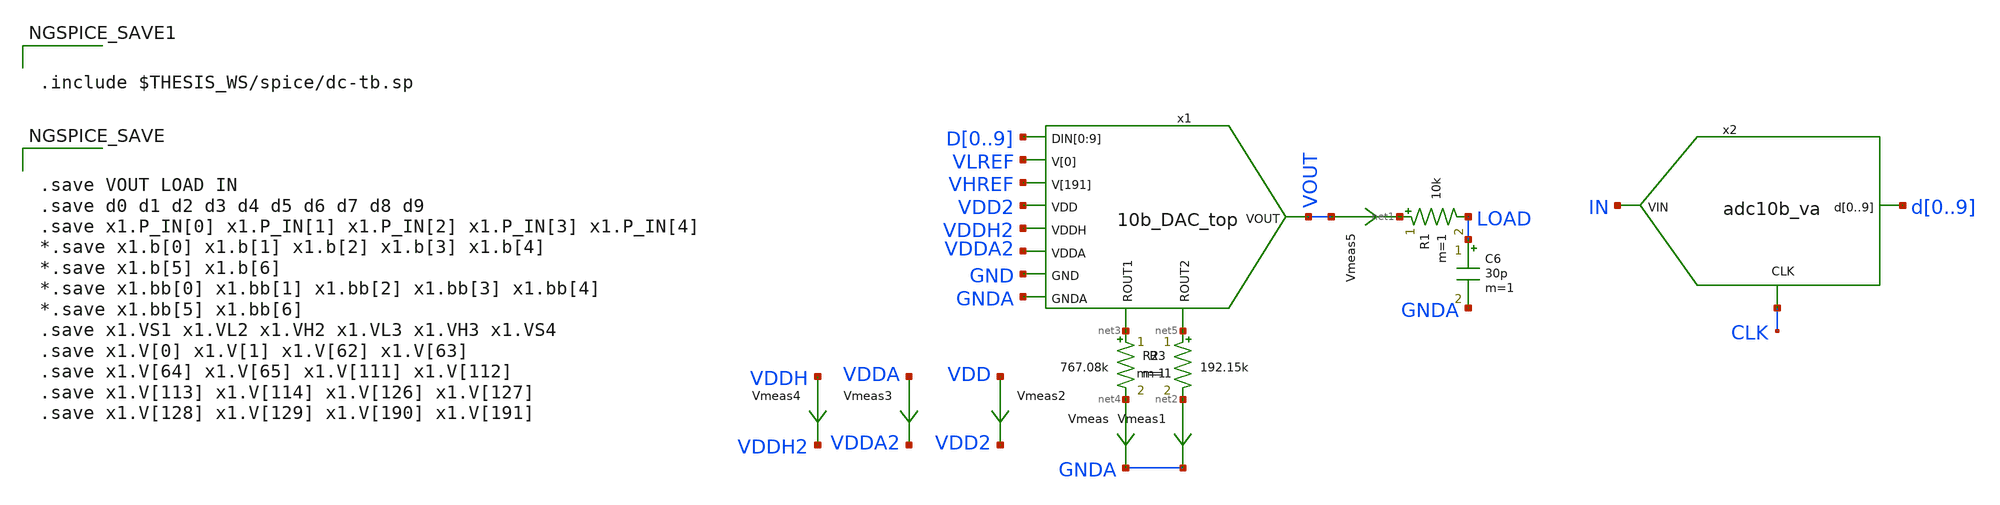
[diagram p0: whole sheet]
** sch_path: xschem/10b_DAC_dc-tb.sch
.lib $::SKYWATER_MODELS/sky130.lib.spice tt
.include $::SKYWATER_STDCELLS/sky130_fd_sc_hd.spice

**.subckt 10b_DAC_dc-tb
C6 LOAD GNDA 30p m=1
R1 net1 LOAD 10k m=1
Vmeas1 net2 GNDA 0
.save i(vmeas1)
R2 net3 net4 767.08k m=1
Vmeas net4 GNDA 0
.save i(vmeas)
R3 net5 net2 192.15k m=1
Vmeas2 VDD VDD2 0
.save i(vmeas2)
x1 D0 D1 D2 D3 D4 D5 D6 D7 D8 D9 VLREF VHREF VDD2 VDDH2 VDDA2 GND GNDA VOUT net3 net5 10b_DAC_top
Vmeas3 VDDA VDDA2 0
.save i(vmeas3)
Vmeas4 VDDH VDDH2 0
.save i(vmeas4)
Vmeas5 VOUT net1 0
.save i(vmeas5)
x2 IN CLK d0 d1 d2 d3 d4 d5 d6 d7 d8 d9 adc10b_va
**** begin user architecture code


.save VOUT LOAD IN
.save d0 d1 d2 d3 d4 d5 d6 d7 d8 d9
.save x1.P_IN[0] x1.P_IN[1] x1.P_IN[2] x1.P_IN[3] x1.P_IN[4]
*.save x1.b[0] x1.b[1] x1.b[2] x1.b[3] x1.b[4]
*.save x1.b[5] x1.b[6]
*.save x1.bb[0] x1.bb[1] x1.bb[2] x1.bb[3] x1.bb[4]
*.save x1.bb[5] x1.bb[6]
.save x1.VS1 x1.VL2 x1.VH2 x1.VL3 x1.VH3 x1.VS4
.save x1.V[0] x1.V[1] x1.V[62] x1.V[63]
.save x1.V[64] x1.V[65] x1.V[111] x1.V[112]
.save x1.V[113] x1.V[114] x1.V[126] x1.V[127]
.save x1.V[128] x1.V[129] x1.V[190] x1.V[191]




.include $THESIS_WS/spice/dc-tb.sp


**** end user architecture code
**.ends
.end
